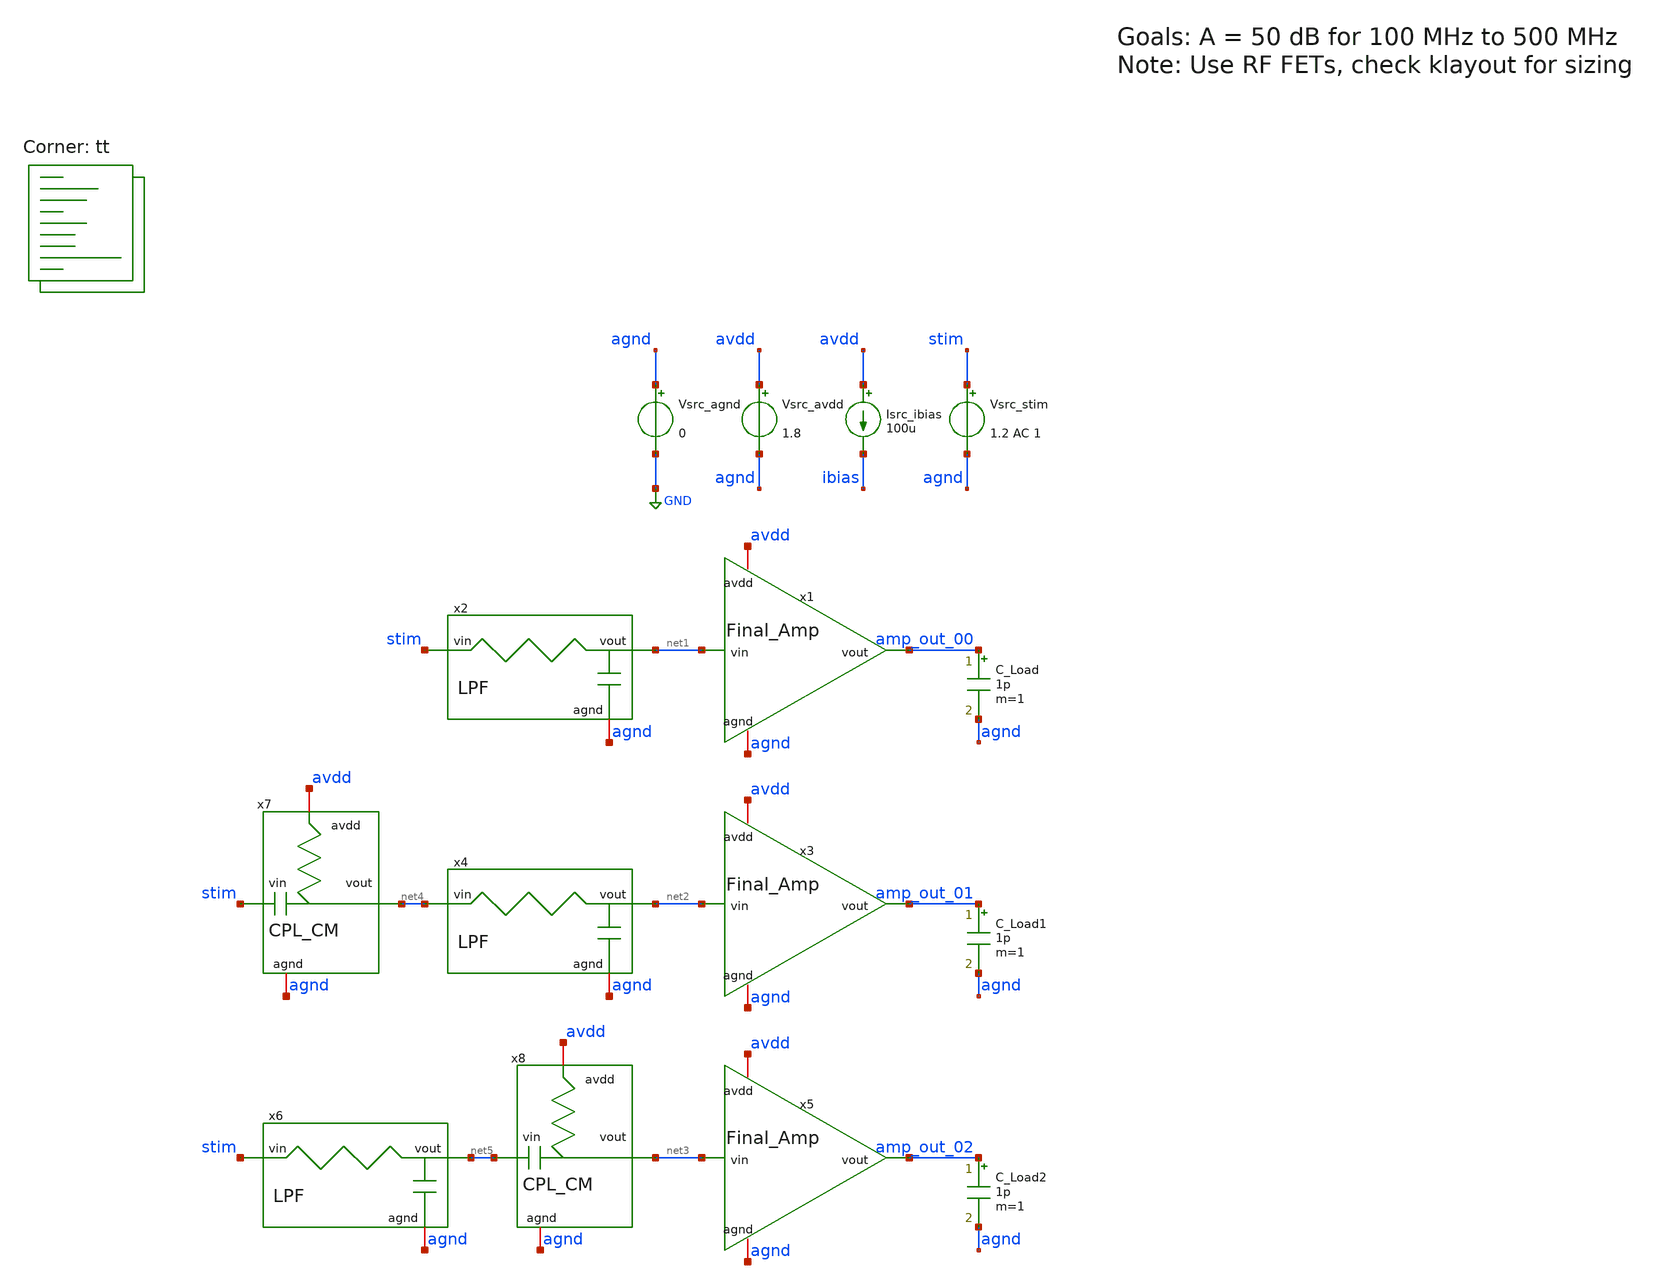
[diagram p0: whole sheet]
** sch_path: AMP/TB_Final_Amp.sch
**.subckt TB_Final_Amp
x1 amp_out_00 net1 agnd avdd Final_Amp
Vsrc_agnd agnd GND 0
Vsrc_avdd avdd agnd 1.8
Vsrc_stim stim agnd 1.2 AC 1
Isrc_ibias avdd ibias 100u
C_Load amp_out_00 agnd 1p m=1
x2 stim net1 agnd LPF
x3 amp_out_01 net2 agnd avdd Final_Amp
C_Load1 amp_out_01 agnd 1p m=1
x4 net4 net2 agnd LPF
x5 amp_out_02 net3 agnd avdd Final_Amp
C_Load2 amp_out_02 agnd 1p m=1
x6 stim net5 agnd LPF
x7 avdd agnd net4 stim CPL_CM
x8 avdd agnd net3 net5 CPL_CM
**** begin user architecture code

* this option enables mos model bin
* selection based on W/NF instead of W


.option savecurrents

.control
save all

op

* Print newline
echo

* Print stats for each MOSFET
* xm1 xm2 xm3 xm4
foreach amp x1 x3 x5
 foreach mos xm1
  * Save stats
  save @m.{$amp}.{$mos}.msky130_fd_pr__nfet_01v8[gm]
  let vth   = @m.{$amp}.{$mos}.msky130_fd_pr__nfet_01v8[vth]
  let vdsat = @m.{$amp}.{$mos}.msky130_fd_pr__nfet_01v8[vdsat]
  let gm    = @m.{$amp}.{$mos}.msky130_fd_pr__nfet_01v8[gm]
  let gds   = @m.{$amp}.{$mos}.msky130_fd_pr__nfet_01v8[gds]

  * Print stats
  echo Stats for $amp $mos:
  print vth
  print vdsat
  print gm
  print gds

  * Print newline
  echo

 end
end

* Print region of operation
echo Regions of Operation:
foreach amp x1 x3 x5
 foreach nmos xm1
  * Save stats
  let vds = @m.{$amp}.{$nmos}.msky130_fd_pr__nfet_01v8[vds]
  let vgs = @m.{$amp}.{$nmos}.msky130_fd_pr__nfet_01v8[vgs]
  let vth = @m.{$amp}.{$nmos}.msky130_fd_pr__nfet_01v8[vth]

  * Check and print regions
  if (vgs <= vth)
   echo $amp $nmos: N Cutoff
  elseif (vds <= (vgs - vth))
   echo $amp $nmos: N Triode
  else
   echo $amp $nmos: N Saturation
  end
 end
end

* Print newline
echo

* Sweep frequency
write TB_Final_Amp.raw
set appendwrite
ac dec 100 1 1e11
remzerovec

* Calculate gain
let ratio_00 = v(amp_out_00)/v(stim)
let ratio_01 = v(amp_out_01)/v(stim)
let ratio_02 = v(amp_out_02)/v(stim)

let gain_00 = db(mag(ratio_00))
let gain_01 = db(mag(ratio_01))
let gain_02 = db(mag(ratio_02))

write TB_Final_Amp.raw

.endc


.lib $::SKYWATER_MODELS/sky130.lib.spice tt
**** end user architecture code
**.ends
.GLOBAL GND
.end
